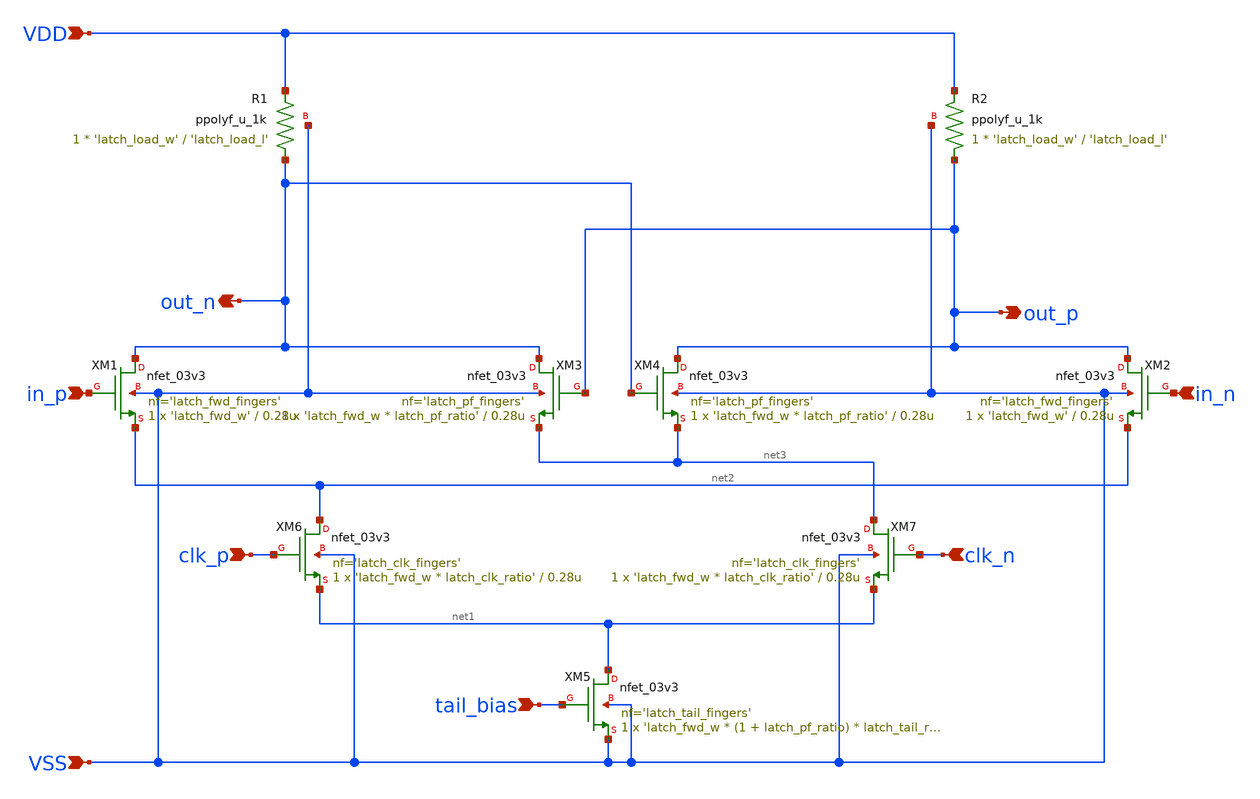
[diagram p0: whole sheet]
** sch_path: xschem/latch_fast.sch
**.subckt latch_fast VSS VDD out_n out_p in_p in_n clk_p clk_n tail_bias
*.ipin VSS
*.ipin VDD
*.opin out_n
*.opin out_p
*.ipin in_p
*.ipin in_n
*.ipin clk_p
*.ipin clk_n
*.ipin tail_bias
XM1 out_n in_p net2 VSS nfet_03v3 L=0.28u W='latch_fwd_w' nf='latch_fwd_fingers' ad='int((nf+1)/2) * W/nf * 0.18u'
+ as='int((nf+2)/2) * W/nf * 0.18u' pd='2*int((nf+1)/2) * (W/nf + 0.18u)' ps='2*int((nf+2)/2) * (W/nf + 0.18u)'
+ nrd='0.18u / W' nrs='0.18u / W' sa=0 sb=0 sd=0 m=1
XM3 out_n out_p net3 VSS nfet_03v3 L=0.28u W='latch_fwd_w * latch_pf_ratio' nf='latch_pf_fingers' ad='int((nf+1)/2) * W/nf * 0.18u'
+ as='int((nf+2)/2) * W/nf * 0.18u' pd='2*int((nf+1)/2) * (W/nf + 0.18u)' ps='2*int((nf+2)/2) * (W/nf + 0.18u)'
+ nrd='0.18u / W' nrs='0.18u / W' sa=0 sb=0 sd=0 m=1
XM4 out_p out_n net3 VSS nfet_03v3 L=0.28u W='latch_fwd_w * latch_pf_ratio' nf='latch_pf_fingers' ad='int((nf+1)/2) * W/nf * 0.18u'
+ as='int((nf+2)/2) * W/nf * 0.18u' pd='2*int((nf+1)/2) * (W/nf + 0.18u)' ps='2*int((nf+2)/2) * (W/nf + 0.18u)'
+ nrd='0.18u / W' nrs='0.18u / W' sa=0 sb=0 sd=0 m=1
XM5 net1 tail_bias VSS VSS nfet_03v3 L='latch_tail_l' W='latch_fwd_w * (1 + latch_pf_ratio) * latch_tail_ratio'
+ nf='latch_tail_fingers' ad='int((nf+1)/2) * W/nf * 0.18u' as='int((nf+2)/2) * W/nf * 0.18u' pd='2*int((nf+1)/2) * (W/nf + 0.18u)'
+ ps='2*int((nf+2)/2) * (W/nf + 0.18u)' nrd='0.18u / W' nrs='0.18u / W' sa=0 sb=0 sd=0 m=1
XM2 out_p in_n net2 VSS nfet_03v3 L=0.28u W='latch_fwd_w' nf='latch_fwd_fingers' ad='int((nf+1)/2) * W/nf * 0.18u'
+ as='int((nf+2)/2) * W/nf * 0.18u' pd='2*int((nf+1)/2) * (W/nf + 0.18u)' ps='2*int((nf+2)/2) * (W/nf + 0.18u)'
+ nrd='0.18u / W' nrs='0.18u / W' sa=0 sb=0 sd=0 m=1
XR1 out_n VDD VSS ppolyf_u_1k r_width='latch_load_w' r_length='latch_load_l' m=1
XR2 out_p VDD VSS ppolyf_u_1k r_width='latch_load_w' r_length='latch_load_l' m=1
XM6 net2 clk_p net1 VSS nfet_03v3 L=0.28u W='latch_fwd_w * latch_clk_ratio' nf='latch_clk_fingers' ad='int((nf+1)/2) * W/nf * 0.18u'
+ as='int((nf+2)/2) * W/nf * 0.18u' pd='2*int((nf+1)/2) * (W/nf + 0.18u)' ps='2*int((nf+2)/2) * (W/nf + 0.18u)'
+ nrd='0.18u / W' nrs='0.18u / W' sa=0 sb=0 sd=0 m=1
XM7 net3 clk_n net1 VSS nfet_03v3 L=0.28u W='latch_fwd_w * latch_clk_ratio' nf='latch_clk_fingers' ad='int((nf+1)/2) * W/nf * 0.18u'
+ as='int((nf+2)/2) * W/nf * 0.18u' pd='2*int((nf+1)/2) * (W/nf + 0.18u)' ps='2*int((nf+2)/2) * (W/nf + 0.18u)'
+ nrd='0.18u / W' nrs='0.18u / W' sa=0 sb=0 sd=0 m=1
**.ends
.end
